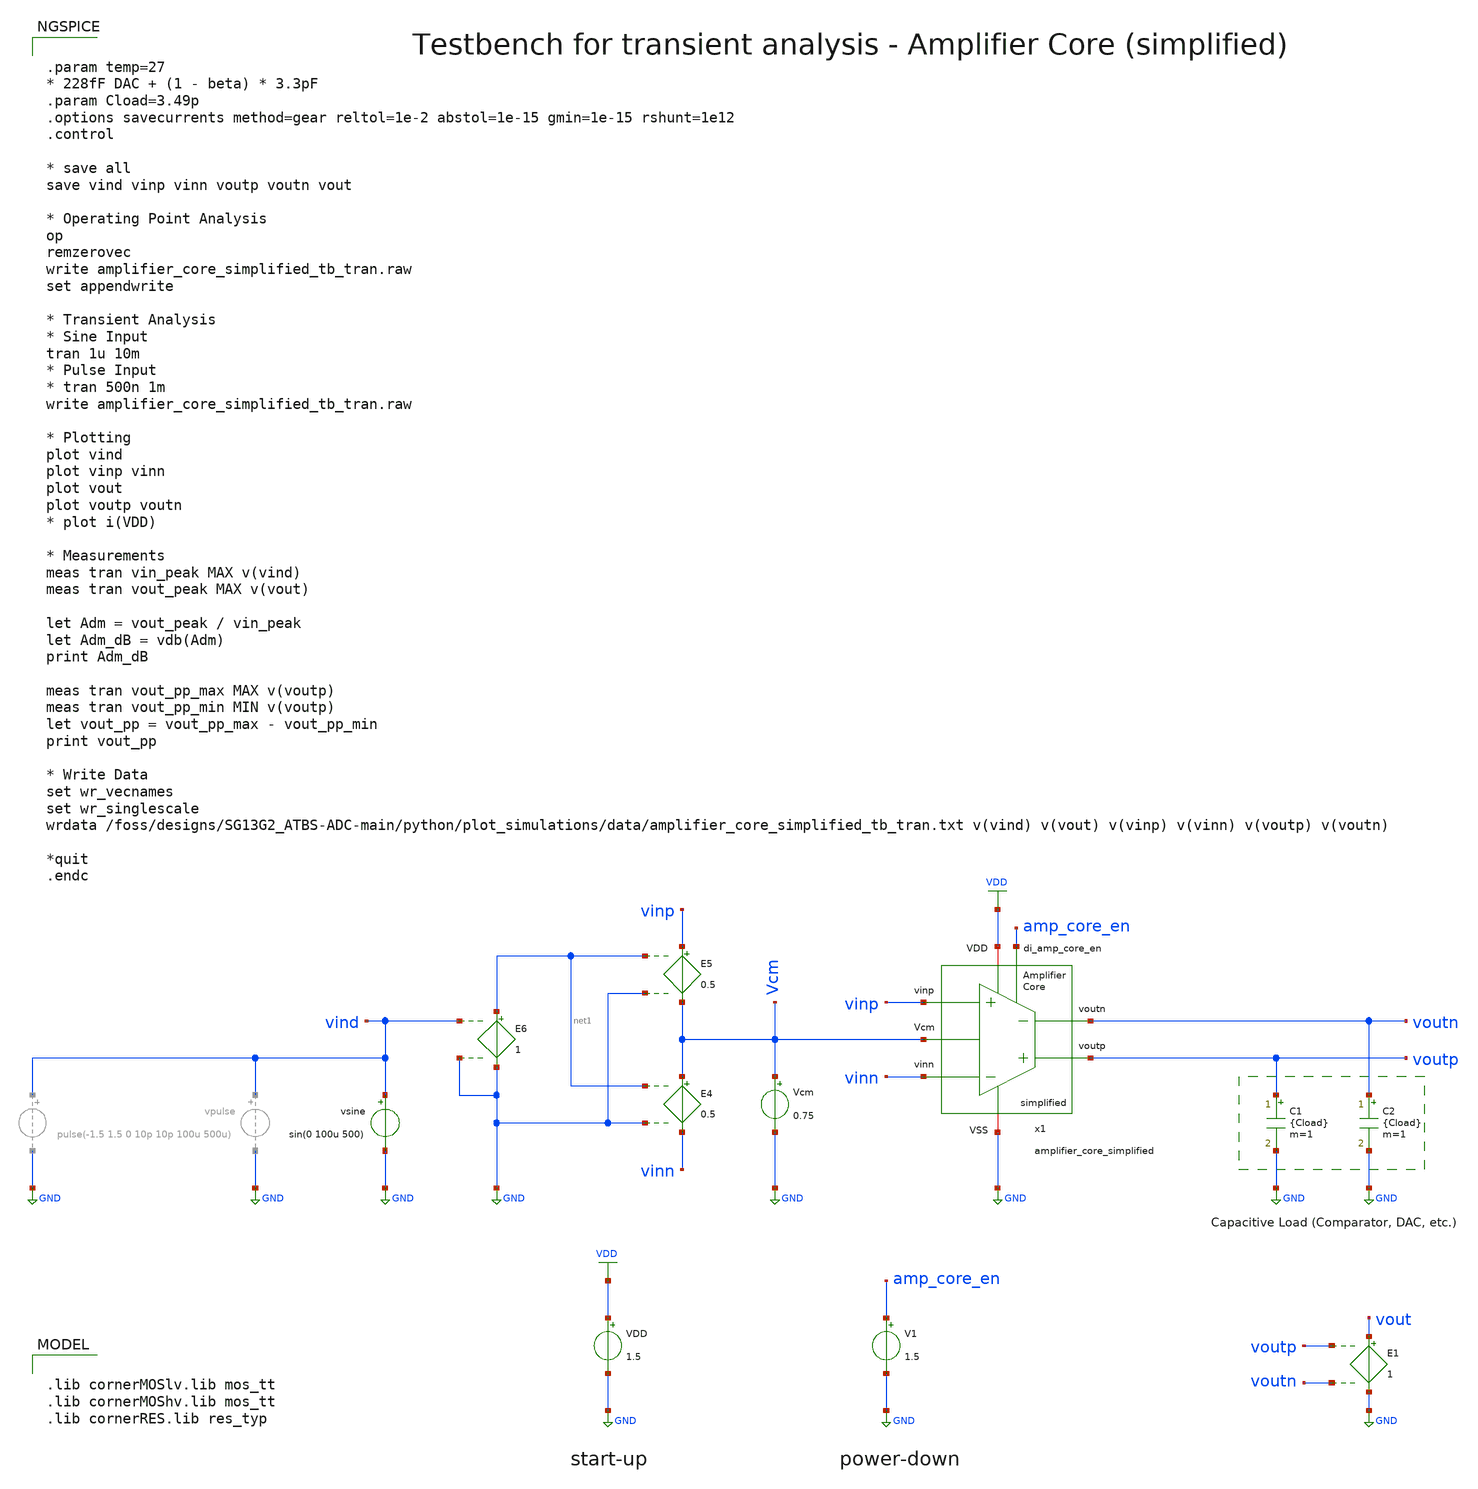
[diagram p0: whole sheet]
** sch_path: SG13G2_ATBS-ADC-main/xschem/bio_amplifier/amplifier_core/testbenches/amplifier_core_simplified_tb_tran.sch
**.subckt amplifier_core_simplified_tb_tran
VDD VDD GND 1.5
C1 voutp GND {Cload} m=1
C2 voutn GND {Cload} m=1
E1 vout GND voutp voutn 1
x1 voutp voutn amp_core_en vinn vinp VDD GND Vcm amplifier_core_simplified
V1 amp_core_en GND 1.5
E4 Vcm vinn net1 GND 0.5
E5 vinp Vcm net1 GND 0.5
E6 net1 GND vind GND 1
vsine vind GND sin(0 100u 500)
Vcm Vcm GND 0.75
**** begin user architecture code


.param temp=27
* 228fF DAC + (1 - beta) * 3.3pF
.param Cload=3.49p
.options savecurrents method=gear reltol=1e-2 abstol=1e-15 gmin=1e-15 rshunt=1e12
.control

* save all
save vind vinp vinn voutp voutn vout

* Operating Point Analysis
op
remzerovec
write amplifier_core_simplified_tb_tran.raw
set appendwrite

* Transient Analysis
* Sine Input
tran 1u 10m
* Pulse Input
* tran 500n 1m
write amplifier_core_simplified_tb_tran.raw

* Plotting
plot vind
plot vinp vinn
plot vout
plot voutp voutn
* plot i(VDD)

* Measurements
meas tran vin_peak MAX v(vind)
meas tran vout_peak MAX v(vout)

let Adm = vout_peak / vin_peak
let Adm_dB = vdb(Adm)
print Adm_dB

meas tran vout_pp_max MAX v(voutp)
meas tran vout_pp_min MIN v(voutp)
let vout_pp = vout_pp_max - vout_pp_min
print vout_pp

* Write Data
set wr_vecnames
set wr_singlescale
wrdata
+ /foss/designs/SG13G2_ATBS-ADC-main/python/plot_simulations/data/amplifier_core_simplified_tb_tran.txt v(vind) v(vout) v(vinp) v(vinn) v(voutp) v(voutn)

*quit
.endc



.lib cornerMOSlv.lib mos_tt
.lib cornerMOShv.lib mos_tt
.lib cornerRES.lib res_typ

**** end user architecture code
**.ends
.GLOBAL GND
.GLOBAL VDD
.end
